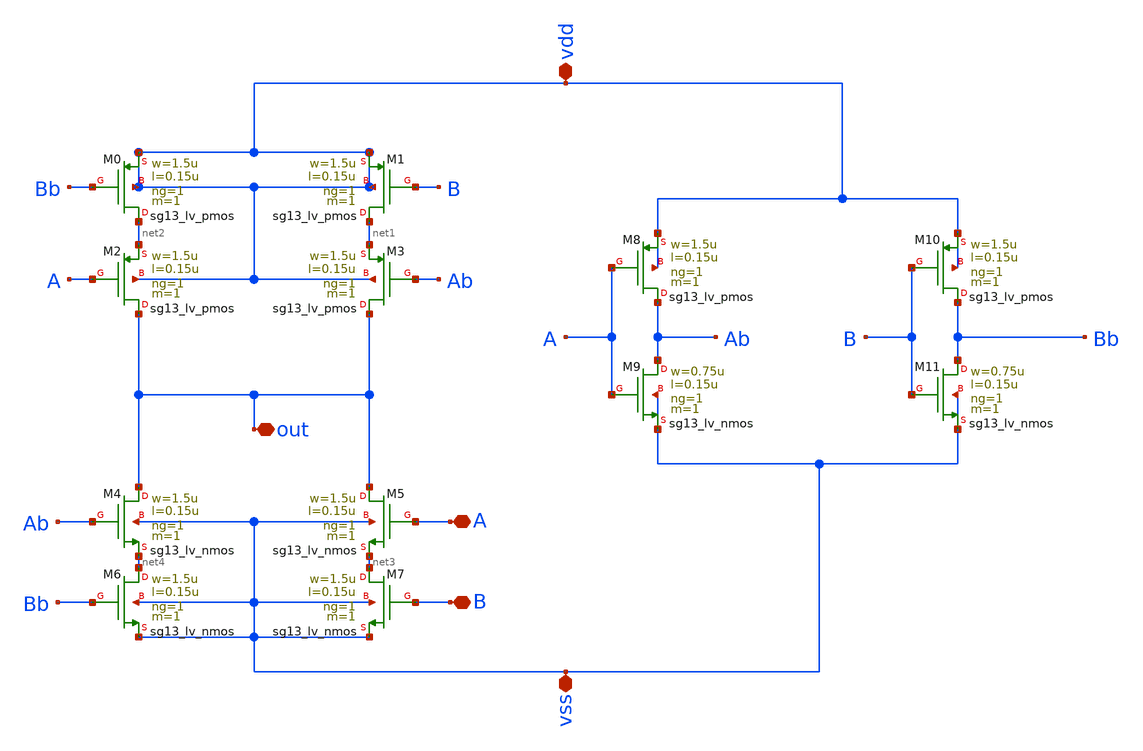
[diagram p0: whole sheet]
** sch_path: design/blocks/xor2/schematic/xor2.sch
**.subckt xor2 vdd vss out B A
*.iopin vdd
*.iopin vss
*.iopin out
*.iopin B
*.iopin A
XM4 out Ab net4 vss sg13_lv_nmos w=1.5u l=0.15u ng=1 m=1 mm_ok=1
XM6 net4 Bb vss vss sg13_lv_nmos w=1.5u l=0.15u ng=1 m=1 mm_ok=1
XM5 out A net3 vss sg13_lv_nmos w=1.5u l=0.15u ng=1 m=1 mm_ok=1
XM7 net3 B vss vss sg13_lv_nmos w=1.5u l=0.15u ng=1 m=1 mm_ok=1
XM9 Ab A vss vss sg13_lv_nmos w=0.75u l=0.15u ng=1 m=1 mm_ok=1
XM11 Bb B vss vss sg13_lv_nmos w=0.75u l=0.15u ng=1 m=1 mm_ok=1
XM2 out A net2 vdd sg13_lv_pmos w=1.5u l=0.15u ng=1 m=1 mm_ok=1
XM0 net2 Bb vdd vdd sg13_lv_pmos w=1.5u l=0.15u ng=1 m=1 mm_ok=1
XM3 out Ab net1 vdd sg13_lv_pmos w=1.5u l=0.15u ng=1 m=1 mm_ok=1
XM1 net1 B vdd vdd sg13_lv_pmos w=1.5u l=0.15u ng=1 m=1 mm_ok=1
XM8 Ab A vdd vdd sg13_lv_pmos w=1.5u l=0.15u ng=1 m=1 mm_ok=1
XM10 Bb B vdd vdd sg13_lv_pmos w=1.5u l=0.15u ng=1 m=1 mm_ok=1
**.ends
.end
